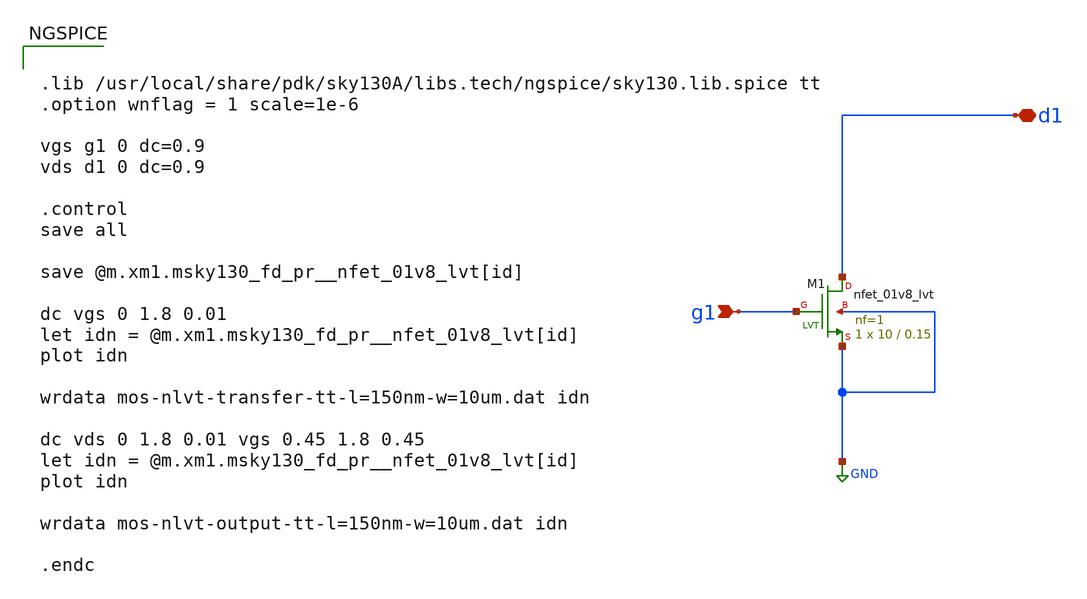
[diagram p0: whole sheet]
** sch_path: cidr/ee-220-activity-4.sch
**.subckt ee-220-activity-4 g1 d1
*.ipin g1
*.iopin d1
XM1 d1 g1 GND GND sky130_fd_pr__nfet_01v8_lvt L=0.15 W=10 nf=1 ad='int((nf+1)/2) * W/nf * 0.29' as='int((nf+2)/2) * W/nf * 0.29'
+ pd='2*int((nf+1)/2) * (W/nf + 0.29)' ps='2*int((nf+2)/2) * (W/nf + 0.29)' nrd='0.29 / W' nrs='0.29 / W'
+ sa=0 sb=0 sd=0 mult=1 m=1
**** begin user architecture code


.lib /usr/local/share/pdk/sky130A/libs.tech/ngspice/sky130.lib.spice tt
.option wnflag = 1 scale=1e-6

vgs g1 0 dc=0.9
vds d1 0 dc=0.9

.control
save all

save @m.xm1.msky130_fd_pr__nfet_01v8_lvt[id]

dc vgs 0 1.8 0.01
let idn = @m.xm1.msky130_fd_pr__nfet_01v8_lvt[id]
plot idn

wrdata mos-nlvt-transfer-tt-l=150nm-w=10um.dat idn

dc vds 0 1.8 0.01 vgs 0.45 1.8 0.45
let idn = @m.xm1.msky130_fd_pr__nfet_01v8_lvt[id]
plot idn

wrdata mos-nlvt-output-tt-l=150nm-w=10um.dat idn

.endc


**** end user architecture code
**.ends
.GLOBAL GND
.end
